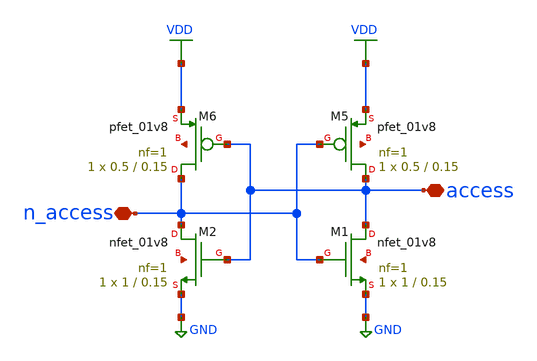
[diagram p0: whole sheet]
** sch_path: analog/schematics/4T.sch
**.subckt 4T access n_access
*.iopin access
*.iopin n_access
XM1 access n_access GND net1 sky130_fd_pr__nfet_01v8 L=0.15 W=1 nf=1 ad='int((nf+1)/2) * W/nf * 0.29'
+ as='int((nf+2)/2) * W/nf * 0.29' pd='2*int((nf+1)/2) * (W/nf + 0.29)' ps='2*int((nf+2)/2) * (W/nf + 0.29)'
+ nrd='0.29 / W' nrs='0.29 / W' sa=0 sb=0 sd=0 mult=1 m=1
XM2 n_access access GND net2 sky130_fd_pr__nfet_01v8 L=0.15 W=1 nf=1 ad='int((nf+1)/2) * W/nf * 0.29'
+ as='int((nf+2)/2) * W/nf * 0.29' pd='2*int((nf+1)/2) * (W/nf + 0.29)' ps='2*int((nf+2)/2) * (W/nf + 0.29)'
+ nrd='0.29 / W' nrs='0.29 / W' sa=0 sb=0 sd=0 mult=1 m=1
XM5 access n_access VDD net3 sky130_fd_pr__pfet_01v8 L=0.15 W=0.5 nf=1 ad='int((nf+1)/2) * W/nf * 0.29'
+ as='int((nf+2)/2) * W/nf * 0.29' pd='2*int((nf+1)/2) * (W/nf + 0.29)' ps='2*int((nf+2)/2) * (W/nf + 0.29)'
+ nrd='0.29 / W' nrs='0.29 / W' sa=0 sb=0 sd=0 mult=1 m=1
XM6 n_access access VDD net4 sky130_fd_pr__pfet_01v8 L=0.15 W=0.5 nf=1 ad='int((nf+1)/2) * W/nf * 0.29'
+ as='int((nf+2)/2) * W/nf * 0.29' pd='2*int((nf+1)/2) * (W/nf + 0.29)' ps='2*int((nf+2)/2) * (W/nf + 0.29)'
+ nrd='0.29 / W' nrs='0.29 / W' sa=0 sb=0 sd=0 mult=1 m=1
**.ends
.GLOBAL VDD
.GLOBAL GND
.end
